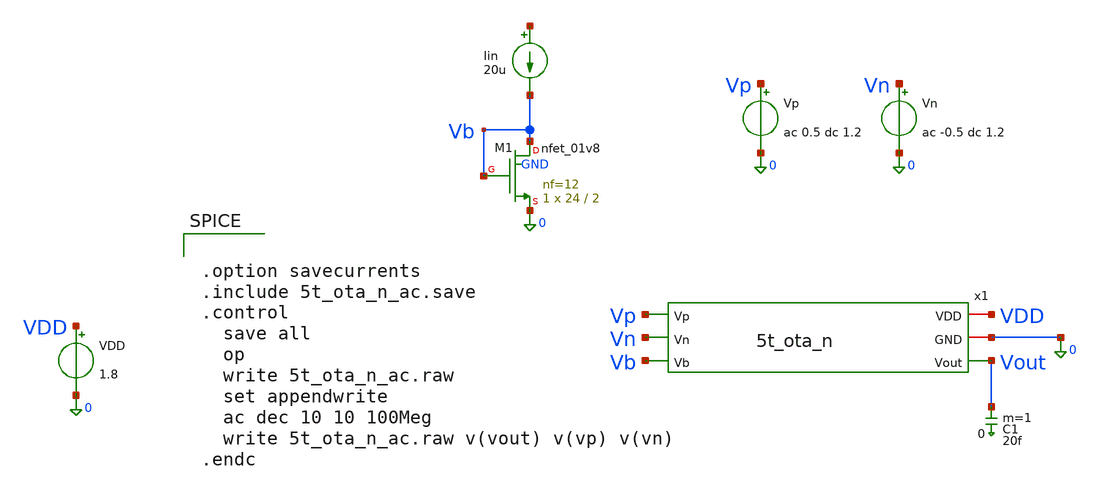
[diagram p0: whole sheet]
** sch_path: sch/archive/old/5t_ota_n_ac.sch
**.subckt 5t_ota_n_ac
Iin net1 Vb 20u
VDD VDD 0 1.8
.save i(vdd)
Vp Vp 0 ac 0.5 dc 1.2
.save i(vp)
Vn Vn 0 ac -0.5 dc 1.2
.save i(vn)
C1 Vout 0 20f m=1
x1 VDD 0 Vp Vn Vb Vout 5t_ota_n
XM1 Vb Vb 0 GND sky130_fd_pr__nfet_01v8 L=2 W=24 nf=12 ad='int((12 + 1)/2) * 24 / 12 * 0.29' as='int((12 + 2)/2) * 24 / 12 * 0.29'
+ pd='2*int((12 + 1)/2) * (24 / 12 + 0.29)' ps='2*int((12 + 2)/2) * (24 / 12 + 0.29)' nrd='0.29 / 24 '
+ nrs='0.29 / 24 ' sa=0 sb=0 sd=0 mult=1 m=1
**** begin user architecture code

** opencircuitdesign pdks install
.lib $::SKYWATER_MODELS/sky130.lib.spice tt
.include $::SKYWATER_STDCELLS/sky130_fd_sc_hd.spice



.option savecurrents
.include 5t_ota_n_ac.save
.control
  save all
  op
  write 5t_ota_n_ac.raw
  set appendwrite
  ac dec 10 10 100Meg
  write 5t_ota_n_ac.raw v(vout) v(vp) v(vn)
.endc


**** end user architecture code
**.ends

* expanding   symbol:  5t_ota_n.sym # of pins=6
** sym_path: sch/archive/old/5t_ota_n.sym
** sch_path: sch/archive/old/5t_ota_n.sch
.subckt 5t_ota_n VDD GND Vp Vn Vb Vout
*.iopin VDD
*.ipin Vp
*.opin Vout
*.iopin GND
*.ipin Vn
*.ipin Vb
XM5 net1 Vp Vx GND sky130_fd_pr__nfet_01v8 L=6 W=24 nf=12 ad='int((12 + 1)/2) * 24 / 12 * 0.29' as='int((12 + 2)/2) * 24 / 12 * 0.29'
+ pd='2*int((12 + 1)/2) * (24 / 12 + 0.29)' ps='2*int((12 + 2)/2) * (24 / 12 + 0.29)' nrd='0.29 / 24 '
+ nrs='0.29 / 24 ' sa=0 sb=0 sd=0 mult=1 m=1
XM7 Vx Vb GND GND sky130_fd_pr__nfet_01v8 L=2 W=24 nf=12 ad='int((12 + 1)/2) * 24 / 12 * 0.29' as='int((12 + 2)/2) * 24 / 12 * 0.29'
+ pd='2*int((12 + 1)/2) * (24 / 12 + 0.29)' ps='2*int((12 + 2)/2) * (24 / 12 + 0.29)' nrd='0.29 / 24 '
+ nrs='0.29 / 24 ' sa=0 sb=0 sd=0 mult=1 m=1
XM8 net1 net1 VDD VDD sky130_fd_pr__pfet_01v8 L=1 W=10 nf=5 ad='int((5 + 1)/2) * 10 / 5 * 0.29' as='int((5 + 2)/2) * 10 / 5 * 0.29'
+ pd='2*int((5 + 1)/2) * (10 / 5 + 0.29)' ps='2*int((5 + 2)/2) * (10 / 5 + 0.29)' nrd='0.29 / 10 ' nrs='0.29 / 10 '
+ sa=0 sb=0 sd=0 mult=1 m=1
XM9 Vout net1 VDD VDD sky130_fd_pr__pfet_01v8 L=1 W=10 nf=5 ad='int((5 + 1)/2) * 10 / 5 * 0.29' as='int((5 + 2)/2) * 10 / 5 * 0.29'
+ pd='2*int((5 + 1)/2) * (10 / 5 + 0.29)' ps='2*int((5 + 2)/2) * (10 / 5 + 0.29)' nrd='0.29 / 10 ' nrs='0.29 / 10 '
+ sa=0 sb=0 sd=0 mult=1 m=1
XM1 Vout Vn Vx GND sky130_fd_pr__nfet_01v8 L=6 W=24 nf=12 ad='int((12 + 1)/2) * 24 / 12 * 0.29' as='int((12 + 2)/2) * 24 / 12 * 0.29'
+ pd='2*int((12 + 1)/2) * (24 / 12 + 0.29)' ps='2*int((12 + 2)/2) * (24 / 12 + 0.29)' nrd='0.29 / 24 '
+ nrs='0.29 / 24 ' sa=0 sb=0 sd=0 mult=1 m=1
.ends

.end
